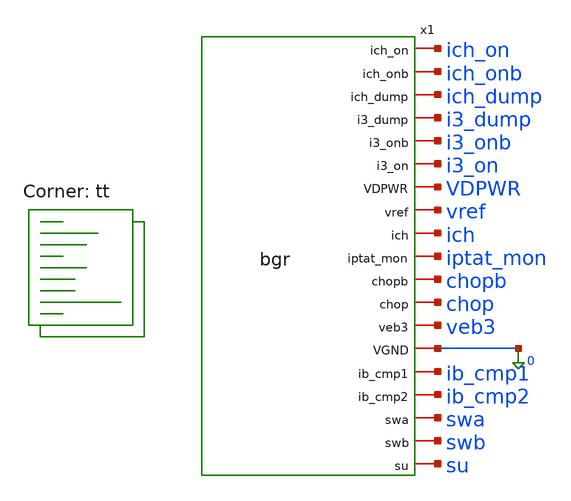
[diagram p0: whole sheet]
** sch_path: xschem/tb_bg_chop.sch
**.subckt tb_bg_chop
x1 ich_on ich_onb ich_dump i3_dump i3_onb i3_on VDPWR vref ich iptat_mon chopb chop veb3 0 ib_cmp1
+ ib_cmp2 swa swb su bgr
**** begin user architecture code
.lib $::SKYWATER_MODELS/sky130.lib.spice tt

*   S0 = normal, S1 = i3_sel 1 (half-current output branch), S2 = ich_sel 1 (half slope)
Vdd VDPWR 0 1.8
Vswa swa 0 1.8
Vswb swb 0 0
Vchop chop 0 0
Vchopb chopb 0 1.8
Vichon ich_on 0 1.8
Vichonb ich_onb 0 0
Vichdump ich_dump 0 0
Vi3on i3_on 0 1.8
Vi3onb i3_onb 0 0
Vi3dump i3_dump 0 0
* parks as in 3d; 2 pF on vref as the spec bench
E4 p4 0 x1.va 0 1
V4 ich p4 0
V7 iptat_mon p4 0
Vc1 ib_cmp1 0 0.70
Vc2 ib_cmp2 0 0.70
Cref vref 0 2p
* the design nodeset
.nodeset v(x1.vpg)=0.55 v(x1.va)=0.71 v(x1.vb)=0.71 v(vref)=1.25
.control
option reltol=1e-6 vntol=1e-9 abstol=1e-15
let vd = 1.8
foreach t -40 -20 0 25 50 75 100 125
  option temp=$t
  * S0: normal
  op
  let ip = 2*i(v7)*1e9
  let ib = abs(@m.x1.xcore.xmnb2.msky130_fd_pr__nfet_01v8[id])*1e9
  let ibr = ib/ip
  let xvref = v(vref)
  let xveb3 = v(veb3)
  let mu = 1 - xveb3/xvref
  let vos = (v(x1.vb)-v(x1.va))*1e6
  let xvpg = v(x1.vpg)
  let tailm = (abs(@m.x1.xota.xmtail.msky130_fd_pr__pfet_01v8[vds]) -
+ abs(@m.x1.xota.xmtail.msky130_fd_pr__pfet_01v8[vdsat]))*1e3
  let p3m = (abs(@m.x1.xcore.x1.xmp3a.msky130_fd_pr__pfet_01v8[vds]) -
+ abs(@m.x1.xcore.x1.xmp3a.msky130_fd_pr__pfet_01v8[vdsat]))*1e3
  let xsu = v(su)*1e3
  let imsu1 = abs(@m.x1.xcore.xsu.xmsu1.msky130_fd_pr__pfet_01v8[id])*1e9
  let imsu2 = abs(@m.x1.xcore.xsu.xmsu2.msky130_fd_pr__nfet_01v8[id])*1e12
  let ich = i(v4)*1e9
  set s0vref = $&xvref
  set s0veb3 = $&xveb3
  set s0ich = $&ich
  let i3s0 = abs(@m.x1.xcore.x1.xmp3a.msky130_fd_pr__pfet_01v8[id]) +
+ abs(@m.x1.xcore.x1.xmp3b.msky130_fd_pr__pfet_01v8[id])
  set s0i3 = $&i3s0
  echo PVT temp=$t Iptat_nA=$&ip IB_ratio=$&ibr vref_V=$&xvref veb3_V=$&xveb3 mu=$&mu vos_uV=$&vos
+ vpg_V=$&xvpg tail_margin_mV=$&tailm p3_margin_mV=$&p3m su_mV=$&xsu Imsu1_nA=$&imsu1 Imsu2_pA=$&imsu2
+ Ich_nA=$&ich
  * 8c: input-switch leakage, state A (S1/S2 on, S3/S4 off): everything hanging on va and vb
  let lva = (abs(@m.x1.xs1.msky130_fd_pr__nfet_01v8_lvt[id]) +
+ abs(@m.x1.xs1.msky130_fd_pr__nfet_01v8_lvt[ibd]) + abs(@m.x1.xs3.msky130_fd_pr__nfet_01v8_lvt[id]) +
+ abs(@m.x1.xs3.msky130_fd_pr__nfet_01v8_lvt[ibd]))*1e12
  let lvb = (abs(@m.x1.xs2.msky130_fd_pr__nfet_01v8_lvt[id]) +
+ abs(@m.x1.xs2.msky130_fd_pr__nfet_01v8_lvt[ibd]) + abs(@m.x1.xs4.msky130_fd_pr__nfet_01v8_lvt[id]) +
+ abs(@m.x1.xs4.msky130_fd_pr__nfet_01v8_lvt[ibd]))*1e12
  let loff = abs(@m.x1.xs3.msky130_fd_pr__nfet_01v8_lvt[id])*1e12
  echo LEAK temp=$t Ileak_va_pA=$&lva Ileak_vb_pA=$&lvb Ioff_channel_S3_pA=$&loff
  * S1: i3_sel = 1 (P3b to ground)
  alter vi3on = 0
  alter vi3onb = $&vd
  alter vi3dump = $&vd
  op
  let i3a = abs(@m.x1.xcore.x1.xmp3a.msky130_fd_pr__pfet_01v8[id])
  let rho = i3a/$s0i3
  let xvref = v(vref)
  let xveb3 = v(veb3)
  let mu = 1 - xveb3/xvref
  let xsu = v(su)*1e3
  let chi = 10*$s0veb3/($s0vref - $s0veb3) - 5*xveb3/(xvref - xveb3) - 1/3
  echo HALF temp=$t rho=$&rho vref_V=$&xvref veb3_V=$&xveb3 mu=$&mu su_mV=$&xsu chi_nom=$&chi
  alter vi3on = $&vd
  alter vi3onb = 0
  alter vi3dump = 0
  * S2: ich_sel = 1 (P4b to ground)
  alter vichon = 0
  alter vichonb = $&vd
  alter vichdump = $&vd
  op
  let ich = i(v4)*1e9
  let ichr = ich/$s0ich
  echo SLOPE temp=$t Ich_nA=$&ich Ich_ratio=$&ichr
  alter vichon = $&vd
  alter vichonb = 0
  alter vichdump = 0
end
.endc

**** end user architecture code
**.ends

* expanding   symbol:  bgr.sym # of pins=19
** sym_path: xschem/bgr.sym
** sch_path: xschem/bgr.sch
.subckt bgr ich_on ich_onb ich_dump i3_dump i3_onb i3_on VDPWR vref ich iptat_mon chopb chop veb3
+ VGND ib_cmp1 ib_cmp2 swa swb su
*.iopin swb
*.iopin VDPWR
*.iopin VGND
*.iopin vref
*.iopin veb3
*.iopin ich
*.iopin iptat_mon
*.iopin ib_cmp1
*.iopin ib_cmp2
*.iopin swa
*.iopin chop
*.iopin chopb
*.iopin ich_on
*.iopin ich_onb
*.iopin ich_dump
*.iopin i3_on
*.iopin i3_onb
*.iopin i3_dump
*.iopin su
xcore vpg VDPWR i3b vref ichb ich vb iptat_mon veb3 VGND va ibias ib_cmp1 ib_cmp2 su bg_core
xota inp inn vpg VDPWR VGND ibias chop chopb ota2s
XS1 va swa inn VGND sky130_fd_pr__nfet_01v8_lvt L=0.5 W=4 nf=1 ad='int((1 + 1)/2) * 4 / 1 * 0.29' as='int((1 + 2)/2) * 4 / 1 * 0.29'
+ pd='2*int((1 + 1)/2) * (4 / 1 + 0.29)' ps='2*int((1 + 2)/2) * (4 / 1 + 0.29)' nrd='0.29 / 4 ' nrs='0.29 / 4 '
+ sa=0 sb=0 sd=0 mult=1 m=1
XS2 vb swa inp VGND sky130_fd_pr__nfet_01v8_lvt L=0.5 W=4 nf=1 ad='int((1 + 1)/2) * 4 / 1 * 0.29' as='int((1 + 2)/2) * 4 / 1 * 0.29'
+ pd='2*int((1 + 1)/2) * (4 / 1 + 0.29)' ps='2*int((1 + 2)/2) * (4 / 1 + 0.29)' nrd='0.29 / 4 ' nrs='0.29 / 4 '
+ sa=0 sb=0 sd=0 mult=1 m=1
XS3 va swb inp VGND sky130_fd_pr__nfet_01v8_lvt L=0.5 W=4 nf=1 ad='int((1 + 1)/2) * 4 / 1 * 0.29' as='int((1 + 2)/2) * 4 / 1 * 0.29'
+ pd='2*int((1 + 1)/2) * (4 / 1 + 0.29)' ps='2*int((1 + 2)/2) * (4 / 1 + 0.29)' nrd='0.29 / 4 ' nrs='0.29 / 4 '
+ sa=0 sb=0 sd=0 mult=1 m=1
XS4 vb swb inn VGND sky130_fd_pr__nfet_01v8_lvt L=0.5 W=4 nf=1 ad='int((1 + 1)/2) * 4 / 1 * 0.29' as='int((1 + 2)/2) * 4 / 1 * 0.29'
+ pd='2*int((1 + 1)/2) * (4 / 1 + 0.29)' ps='2*int((1 + 2)/2) * (4 / 1 + 0.29)' nrd='0.29 / 4 ' nrs='0.29 / 4 '
+ sa=0 sb=0 sd=0 mult=1 m=1
XS_ichon_n ichb ich_on ich VGND sky130_fd_pr__nfet_01v8 L=0.5 W=2 nf=1 ad='int((1 + 1)/2) * 2 / 1 * 0.29'
+ as='int((1 + 2)/2) * 2 / 1 * 0.29' pd='2*int((1 + 1)/2) * (2 / 1 + 0.29)' ps='2*int((1 + 2)/2) * (2 / 1 + 0.29)'
+ nrd='0.29 / 2 ' nrs='0.29 / 2 ' sa=0 sb=0 sd=0 mult=1 m=1
XS_ichon_p ichb ich_onb ich VDPWR sky130_fd_pr__pfet_01v8 L=0.5 W=4 nf=1 ad='int((1 + 1)/2) * 4 / 1 * 0.29'
+ as='int((1 + 2)/2) * 4 / 1 * 0.29' pd='2*int((1 + 1)/2) * (4 / 1 + 0.29)' ps='2*int((1 + 2)/2) * (4 / 1 + 0.29)'
+ nrd='0.29 / 4 ' nrs='0.29 / 4 ' sa=0 sb=0 sd=0 mult=1 m=1
XS_ichdump ichb ich_dump VGND VGND sky130_fd_pr__nfet_01v8 L=0.5 W=1 nf=1 ad='int((1 + 1)/2) * 1 / 1 * 0.29'
+ as='int((1 + 2)/2) * 1 / 1 * 0.29' pd='2*int((1 + 1)/2) * (1 / 1 + 0.29)' ps='2*int((1 + 2)/2) * (1 / 1 + 0.29)'
+ nrd='0.29 / 1 ' nrs='0.29 / 1 ' sa=0 sb=0 sd=0 mult=1 m=1
XS_i3on_n i3b i3_on vref VGND sky130_fd_pr__nfet_01v8 L=0.5 W=2 nf=1 ad='int((1 + 1)/2) * 2 / 1 * 0.29'
+ as='int((1 + 2)/2) * 2 / 1 * 0.29' pd='2*int((1 + 1)/2) * (2 / 1 + 0.29)' ps='2*int((1 + 2)/2) * (2 / 1 + 0.29)'
+ nrd='0.29 / 2 ' nrs='0.29 / 2 ' sa=0 sb=0 sd=0 mult=1 m=1
XS_i3on_p i3b i3_onb vref VDPWR sky130_fd_pr__pfet_01v8 L=0.5 W=4 nf=1 ad='int((1 + 1)/2) * 4 / 1 * 0.29'
+ as='int((1 + 2)/2) * 4 / 1 * 0.29' pd='2*int((1 + 1)/2) * (4 / 1 + 0.29)' ps='2*int((1 + 2)/2) * (4 / 1 + 0.29)'
+ nrd='0.29 / 4 ' nrs='0.29 / 4 ' sa=0 sb=0 sd=0 mult=1 m=1
XS_i3dump i3b i3_dump VGND VGND sky130_fd_pr__nfet_01v8 L=0.5 W=1 nf=1 ad='int((1 + 1)/2) * 1 / 1 * 0.29'
+ as='int((1 + 2)/2) * 1 / 1 * 0.29' pd='2*int((1 + 1)/2) * (1 / 1 + 0.29)' ps='2*int((1 + 2)/2) * (1 / 1 + 0.29)'
+ nrd='0.29 / 1 ' nrs='0.29 / 1 ' sa=0 sb=0 sd=0 mult=1 m=1
.ends


* expanding   symbol:  bg_core.sym # of pins=15
** sym_path: xschem/bg_core.sym
** sch_path: xschem/bg_core.sch
.subckt bg_core vpg VDPWR i3b vref ichb ich vb iptat_mon veb3 VGND va ibias ib_cmp1 ib_cmp2 su
*.iopin va
*.iopin vb
*.iopin vref
*.iopin veb3
*.iopin vpg
*.iopin i3b
*.iopin VDPWR
*.iopin ichb
*.iopin ich
*.iopin iptat_mon
*.iopin ibias
*.iopin ib_cmp1
*.iopin ib_cmp2
*.iopin VGND
*.iopin su
x1 vpg VDPWR i3b vref ichb ich vb iptat_mon nb va bg_mirror
x2 vb vref veb3 VGND eb2 bg_rrow
x3 va veb3 eb2 VGND bg_pnp
XMNB1 nb nb VGND VGND sky130_fd_pr__nfet_01v8 L=8 W=4 nf=1 ad='int((1 + 1)/2) * 4 / 1 * 0.29' as='int((1 + 2)/2) * 4 / 1 * 0.29'
+ pd='2*int((1 + 1)/2) * (4 / 1 + 0.29)' ps='2*int((1 + 2)/2) * (4 / 1 + 0.29)' nrd='0.29 / 4 ' nrs='0.29 / 4 '
+ sa=0 sb=0 sd=0 mult=1 m=1
XMNB2 ibias nb VGND VGND sky130_fd_pr__nfet_01v8 L=8 W=4 nf=1 ad='int((1 + 1)/2) * 4 / 1 * 0.29' as='int((1 + 2)/2) * 4 / 1 * 0.29'
+ pd='2*int((1 + 1)/2) * (4 / 1 + 0.29)' ps='2*int((1 + 2)/2) * (4 / 1 + 0.29)' nrd='0.29 / 4 ' nrs='0.29 / 4 '
+ sa=0 sb=0 sd=0 mult=1 m=1
XMNB3 ib_cmp1 nb VGND VGND sky130_fd_pr__nfet_01v8 L=8 W=4 nf=1 ad='int((1 + 1)/2) * 4 / 1 * 0.29' as='int((1 + 2)/2) * 4 / 1 * 0.29'
+ pd='2*int((1 + 1)/2) * (4 / 1 + 0.29)' ps='2*int((1 + 2)/2) * (4 / 1 + 0.29)' nrd='0.29 / 4 ' nrs='0.29 / 4 '
+ sa=0 sb=0 sd=0 mult=4 m=4
XMNB4 ib_cmp2 nb VGND VGND sky130_fd_pr__nfet_01v8 L=8 W=4 nf=1 ad='int((1 + 1)/2) * 4 / 1 * 0.29' as='int((1 + 2)/2) * 4 / 1 * 0.29'
+ pd='2*int((1 + 1)/2) * (4 / 1 + 0.29)' ps='2*int((1 + 2)/2) * (4 / 1 + 0.29)' nrd='0.29 / 4 ' nrs='0.29 / 4 '
+ sa=0 sb=0 sd=0 mult=4 m=4
xsu VDPWR vref vpg su VGND nb bg_su
.ends


* expanding   symbol:  ota2s.sym # of pins=8
** sym_path: xschem/ota2s.sym
** sch_path: xschem/ota2s.sch
.subckt ota2s INP INN OUT VDPWR VGND IBIAS CHOP CHOPB
*.ipin INN
*.ipin INP
*.ipin IBIAS
*.opin OUT
*.iopin VDPWR
*.iopin VGND
*.ipin CHOPB
*.ipin CHOP
XMREF IBIAS IBIAS VDPWR VDPWR sky130_fd_pr__pfet_01v8 L=4 W=20 nf=1 ad='int((1 + 1)/2) * 20 / 1 * 0.29'
+ as='int((1 + 2)/2) * 20 / 1 * 0.29' pd='2*int((1 + 1)/2) * (20 / 1 + 0.29)' ps='2*int((1 + 2)/2) * (20 / 1 + 0.29)'
+ nrd='0.29 / 20 ' nrs='0.29 / 20 ' sa=0 sb=0 sd=0 mult=1 m=1
XMTAIL tail IBIAS VDPWR VDPWR sky130_fd_pr__pfet_01v8 L=4 W=20 nf=1 ad='int((1 + 1)/2) * 20 / 1 * 0.29'
+ as='int((1 + 2)/2) * 20 / 1 * 0.29' pd='2*int((1 + 1)/2) * (20 / 1 + 0.29)' ps='2*int((1 + 2)/2) * (20 / 1 + 0.29)'
+ nrd='0.29 / 20 ' nrs='0.29 / 20 ' sa=0 sb=0 sd=0 mult=2 m=2
XMP1 d1 INN tail VDPWR sky130_fd_pr__pfet_01v8_lvt L=6 W=25 nf=1 ad='int((1 + 1)/2) * 25 / 1 * 0.29'
+ as='int((1 + 2)/2) * 25 / 1 * 0.29' pd='2*int((1 + 1)/2) * (25 / 1 + 0.29)' ps='2*int((1 + 2)/2) * (25 / 1 + 0.29)'
+ nrd='0.29 / 25 ' nrs='0.29 / 25 ' sa=0 sb=0 sd=0 mult=24 m=24
XMP2 x1 INP tail VDPWR sky130_fd_pr__pfet_01v8_lvt L=6 W=25 nf=1 ad='int((1 + 1)/2) * 25 / 1 * 0.29'
+ as='int((1 + 2)/2) * 25 / 1 * 0.29' pd='2*int((1 + 1)/2) * (25 / 1 + 0.29)' ps='2*int((1 + 2)/2) * (25 / 1 + 0.29)'
+ nrd='0.29 / 25 ' nrs='0.29 / 25 ' sa=0 sb=0 sd=0 mult=24 m=24
XMN1 d1 g12 VGND VGND sky130_fd_pr__nfet_01v8 L=20 W=6 nf=1 ad='int((1 + 1)/2) * 6 / 1 * 0.29' as='int((1 + 2)/2) * 6 / 1 * 0.29'
+ pd='2*int((1 + 1)/2) * (6 / 1 + 0.29)' ps='2*int((1 + 2)/2) * (6 / 1 + 0.29)' nrd='0.29 / 6 ' nrs='0.29 / 6 '
+ sa=0 sb=0 sd=0 mult=2 m=2
XMN2 x1 g12 VGND VGND sky130_fd_pr__nfet_01v8 L=20 W=6 nf=1 ad='int((1 + 1)/2) * 6 / 1 * 0.29' as='int((1 + 2)/2) * 6 / 1 * 0.29'
+ pd='2*int((1 + 1)/2) * (6 / 1 + 0.29)' ps='2*int((1 + 2)/2) * (6 / 1 + 0.29)' nrd='0.29 / 6 ' nrs='0.29 / 6 '
+ sa=0 sb=0 sd=0 mult=2 m=2
XMP3 OUT IBIAS VDPWR VDPWR sky130_fd_pr__pfet_01v8 L=4 W=20 nf=1 ad='int((1 + 1)/2) * 20 / 1 * 0.29'
+ as='int((1 + 2)/2) * 20 / 1 * 0.29' pd='2*int((1 + 1)/2) * (20 / 1 + 0.29)' ps='2*int((1 + 2)/2) * (20 / 1 + 0.29)'
+ nrd='0.29 / 20 ' nrs='0.29 / 20 ' sa=0 sb=0 sd=0 mult=6 m=6
XMN3 OUT g3 VGND VGND sky130_fd_pr__nfet_01v8 L=1 W=7 nf=1 ad='int((1 + 1)/2) * 7 / 1 * 0.29' as='int((1 + 2)/2) * 7 / 1 * 0.29'
+ pd='2*int((1 + 1)/2) * (7 / 1 + 0.29)' ps='2*int((1 + 2)/2) * (7 / 1 + 0.29)' nrd='0.29 / 7 ' nrs='0.29 / 7 '
+ sa=0 sb=0 sd=0 mult=1 m=1
XRZ1 net1 g3 VGND sky130_fd_pr__res_high_po_1p41 L=20 mult=1 m=1
XRZ2 net2 net1 VGND sky130_fd_pr__res_high_po_1p41 L=20 mult=1 m=1
XRZ3 net3 net2 VGND sky130_fd_pr__res_high_po_1p41 L=20 mult=1 m=1
XRZ4 net4 net3 VGND sky130_fd_pr__res_high_po_1p41 L=20 mult=1 m=1
XRZ5 net5 net4 VGND sky130_fd_pr__res_high_po_1p41 L=20 mult=1 m=1
XRZ6 cz net5 VGND sky130_fd_pr__res_high_po_1p41 L=20 mult=1 m=1
XCC cz OUT sky130_fd_pr__cap_mim_m3_1 W=25 L=25 MF=8 m=8
XDP tail VDPWR tail VDPWR sky130_fd_pr__pfet_01v8_lvt L=6 W=25 nf=1 ad='int((1 + 1)/2) * 25 / 1 * 0.29'
+ as='int((1 + 2)/2) * 25 / 1 * 0.29' pd='2*int((1 + 1)/2) * (25 / 1 + 0.29)' ps='2*int((1 + 2)/2) * (25 / 1 + 0.29)'
+ nrd='0.29 / 25 ' nrs='0.29 / 25 ' sa=0 sb=0 sd=0 mult=8 m=8
XDNA d1 VGND VGND VGND sky130_fd_pr__nfet_01v8 L=20 W=6 nf=1 ad='int((1 + 1)/2) * 6 / 1 * 0.29' as='int((1 + 2)/2) * 6 / 1 * 0.29'
+ pd='2*int((1 + 1)/2) * (6 / 1 + 0.29)' ps='2*int((1 + 2)/2) * (6 / 1 + 0.29)' nrd='0.29 / 6 ' nrs='0.29 / 6 '
+ sa=0 sb=0 sd=0 mult=2 m=2
XDNB x1 VGND VGND VGND sky130_fd_pr__nfet_01v8 L=20 W=6 nf=1 ad='int((1 + 1)/2) * 6 / 1 * 0.29' as='int((1 + 2)/2) * 6 / 1 * 0.29'
+ pd='2*int((1 + 1)/2) * (6 / 1 + 0.29)' ps='2*int((1 + 2)/2) * (6 / 1 + 0.29)' nrd='0.29 / 6 ' nrs='0.29 / 6 '
+ sa=0 sb=0 sd=0 mult=2 m=2
XDB VDPWR VDPWR VDPWR VDPWR sky130_fd_pr__pfet_01v8 L=4 W=20 nf=1 ad='int((1 + 1)/2) * 20 / 1 * 0.29'
+ as='int((1 + 2)/2) * 20 / 1 * 0.29' pd='2*int((1 + 1)/2) * (20 / 1 + 0.29)' ps='2*int((1 + 2)/2) * (20 / 1 + 0.29)'
+ nrd='0.29 / 20 ' nrs='0.29 / 20 ' sa=0 sb=0 sd=0 mult=2 m=2
XRD1 VGND VGND VGND sky130_fd_pr__res_high_po_1p41 L=20 mult=1 m=1
XRD2 VGND VGND VGND sky130_fd_pr__res_high_po_1p41 L=20 mult=1 m=1
XSD1 d1 CHOPB g12 VGND sky130_fd_pr__nfet_01v8 L=0.5 W=6 nf=1 ad='int((1 + 1)/2) * 6 / 1 * 0.29' as='int((1 + 2)/2) * 6 / 1 * 0.29'
+ pd='2*int((1 + 1)/2) * (6 / 1 + 0.29)' ps='2*int((1 + 2)/2) * (6 / 1 + 0.29)' nrd='0.29 / 6 ' nrs='0.29 / 6 '
+ sa=0 sb=0 sd=0 mult=1 m=1
XSD2 x1 CHOP g12 VGND sky130_fd_pr__nfet_01v8 L=0.5 W=6 nf=1 ad='int((1 + 1)/2) * 6 / 1 * 0.29' as='int((1 + 2)/2) * 6 / 1 * 0.29'
+ pd='2*int((1 + 1)/2) * (6 / 1 + 0.29)' ps='2*int((1 + 2)/2) * (6 / 1 + 0.29)' nrd='0.29 / 6 ' nrs='0.29 / 6 '
+ sa=0 sb=0 sd=0 mult=1 m=1
XSG2 g3 CHOP d1 VGND sky130_fd_pr__nfet_01v8 L=0.5 W=6 nf=1 ad='int((1 + 1)/2) * 6 / 1 * 0.29' as='int((1 + 2)/2) * 6 / 1 * 0.29'
+ pd='2*int((1 + 1)/2) * (6 / 1 + 0.29)' ps='2*int((1 + 2)/2) * (6 / 1 + 0.29)' nrd='0.29 / 6 ' nrs='0.29 / 6 '
+ sa=0 sb=0 sd=0 mult=1 m=1
XSG1 x1 CHOPB g3 VGND sky130_fd_pr__nfet_01v8 L=0.5 W=6 nf=1 ad='int((1 + 1)/2) * 6 / 1 * 0.29' as='int((1 + 2)/2) * 6 / 1 * 0.29'
+ pd='2*int((1 + 1)/2) * (6 / 1 + 0.29)' ps='2*int((1 + 2)/2) * (6 / 1 + 0.29)' nrd='0.29 / 6 ' nrs='0.29 / 6 '
+ sa=0 sb=0 sd=0 mult=1 m=1
.ends


* expanding   symbol:  bg_mirror.sym # of pins=10
** sym_path: xschem/bg_mirror.sym
** sch_path: xschem/bg_mirror.sch
.subckt bg_mirror vpg VDPWR d3b d3a d4b d4a d2 d7 d5 d1
*.iopin vpg
*.iopin VDPWR
*.iopin d1
*.iopin d2
*.iopin d3a
*.iopin d3b
*.iopin d4a
*.iopin d4b
*.iopin d7
*.iopin d5
XMP1 d1 vpg VDPWR VDPWR sky130_fd_pr__pfet_01v8 L=20 W=8.8 nf=1 ad='int((1 + 1)/2) * 8.8 / 1 * 0.29'
+ as='int((1 + 2)/2) * 8.8 / 1 * 0.29' pd='2*int((1 + 1)/2) * (8.8 / 1 + 0.29)' ps='2*int((1 + 2)/2) * (8.8 / 1 + 0.29)'
+ nrd='0.29 / 8.8 ' nrs='0.29 / 8.8 ' sa=0 sb=0 sd=0 mult=4 m=4
XMP2 d2 vpg VDPWR VDPWR sky130_fd_pr__pfet_01v8 L=20 W=8.8 nf=1 ad='int((1 + 1)/2) * 8.8 / 1 * 0.29'
+ as='int((1 + 2)/2) * 8.8 / 1 * 0.29' pd='2*int((1 + 1)/2) * (8.8 / 1 + 0.29)' ps='2*int((1 + 2)/2) * (8.8 / 1 + 0.29)'
+ nrd='0.29 / 8.8 ' nrs='0.29 / 8.8 ' sa=0 sb=0 sd=0 mult=4 m=4
XMP3A d3a vpg VDPWR VDPWR sky130_fd_pr__pfet_01v8 L=20 W=8.8 nf=1 ad='int((1 + 1)/2) * 8.8 / 1 * 0.29'
+ as='int((1 + 2)/2) * 8.8 / 1 * 0.29' pd='2*int((1 + 1)/2) * (8.8 / 1 + 0.29)' ps='2*int((1 + 2)/2) * (8.8 / 1 + 0.29)'
+ nrd='0.29 / 8.8 ' nrs='0.29 / 8.8 ' sa=0 sb=0 sd=0 mult=2 m=2
XMP3B d3b vpg VDPWR VDPWR sky130_fd_pr__pfet_01v8 L=20 W=8.8 nf=1 ad='int((1 + 1)/2) * 8.8 / 1 * 0.29'
+ as='int((1 + 2)/2) * 8.8 / 1 * 0.29' pd='2*int((1 + 1)/2) * (8.8 / 1 + 0.29)' ps='2*int((1 + 2)/2) * (8.8 / 1 + 0.29)'
+ nrd='0.29 / 8.8 ' nrs='0.29 / 8.8 ' sa=0 sb=0 sd=0 mult=2 m=2
XMP4A d4a vpg VDPWR VDPWR sky130_fd_pr__pfet_01v8 L=20 W=8.8 nf=1 ad='int((1 + 1)/2) * 8.8 / 1 * 0.29'
+ as='int((1 + 2)/2) * 8.8 / 1 * 0.29' pd='2*int((1 + 1)/2) * (8.8 / 1 + 0.29)' ps='2*int((1 + 2)/2) * (8.8 / 1 + 0.29)'
+ nrd='0.29 / 8.8 ' nrs='0.29 / 8.8 ' sa=0 sb=0 sd=0 mult=1 m=1
XMP4B d4b vpg VDPWR VDPWR sky130_fd_pr__pfet_01v8 L=20 W=8.8 nf=1 ad='int((1 + 1)/2) * 8.8 / 1 * 0.29'
+ as='int((1 + 2)/2) * 8.8 / 1 * 0.29' pd='2*int((1 + 1)/2) * (8.8 / 1 + 0.29)' ps='2*int((1 + 2)/2) * (8.8 / 1 + 0.29)'
+ nrd='0.29 / 8.8 ' nrs='0.29 / 8.8 ' sa=0 sb=0 sd=0 mult=1 m=1
XMP7 d7 vpg VDPWR VDPWR sky130_fd_pr__pfet_01v8 L=20 W=8.8 nf=1 ad='int((1 + 1)/2) * 8.8 / 1 * 0.29'
+ as='int((1 + 2)/2) * 8.8 / 1 * 0.29' pd='2*int((1 + 1)/2) * (8.8 / 1 + 0.29)' ps='2*int((1 + 2)/2) * (8.8 / 1 + 0.29)'
+ nrd='0.29 / 8.8 ' nrs='0.29 / 8.8 ' sa=0 sb=0 sd=0 mult=2 m=2
XMP5 d5 vpg VDPWR VDPWR sky130_fd_pr__pfet_01v8 L=20 W=8.8 nf=1 ad='int((1 + 1)/2) * 8.8 / 1 * 0.29'
+ as='int((1 + 2)/2) * 8.8 / 1 * 0.29' pd='2*int((1 + 1)/2) * (8.8 / 1 + 0.29)' ps='2*int((1 + 2)/2) * (8.8 / 1 + 0.29)'
+ nrd='0.29 / 8.8 ' nrs='0.29 / 8.8 ' sa=0 sb=0 sd=0 mult=2 m=2
.ends


* expanding   symbol:  bg_rrow.sym # of pins=5
** sym_path: xschem/bg_rrow.sym
** sch_path: xschem/bg_rrow.sch
.subckt bg_rrow vb vref veb3 VGND eb2
*.iopin vb
*.iopin eb2
*.iopin vref
*.iopin veb3
*.iopin VGND
XR1_1 eb2 net1 VGND sky130_fd_pr__res_high_po_1p41 L=20 mult=1 m=1
XR1_2 net1 net2 VGND sky130_fd_pr__res_high_po_1p41 L=20 mult=1 m=1
XR1_3 net2 net3 VGND sky130_fd_pr__res_high_po_1p41 L=20 mult=1 m=1
XR1_4 net3 vb VGND sky130_fd_pr__res_high_po_1p41 L=20 mult=1 m=1
XR3[39] r3n[38] vref VGND sky130_fd_pr__res_high_po_1p41 L=20 mult=1 m=1
XR3[38] r3n[37] r3n[38] VGND sky130_fd_pr__res_high_po_1p41 L=20 mult=1 m=1
XR3[37] r3n[36] r3n[37] VGND sky130_fd_pr__res_high_po_1p41 L=20 mult=1 m=1
XR3[36] r3n[35] r3n[36] VGND sky130_fd_pr__res_high_po_1p41 L=20 mult=1 m=1
XR3[35] r3n[34] r3n[35] VGND sky130_fd_pr__res_high_po_1p41 L=20 mult=1 m=1
XR3[34] r3n[33] r3n[34] VGND sky130_fd_pr__res_high_po_1p41 L=20 mult=1 m=1
XR3[33] r3n[32] r3n[33] VGND sky130_fd_pr__res_high_po_1p41 L=20 mult=1 m=1
XR3[32] r3n[31] r3n[32] VGND sky130_fd_pr__res_high_po_1p41 L=20 mult=1 m=1
XR3[31] r3n[30] r3n[31] VGND sky130_fd_pr__res_high_po_1p41 L=20 mult=1 m=1
XR3[30] r3n[29] r3n[30] VGND sky130_fd_pr__res_high_po_1p41 L=20 mult=1 m=1
XR3[29] r3n[28] r3n[29] VGND sky130_fd_pr__res_high_po_1p41 L=20 mult=1 m=1
XR3[28] r3n[27] r3n[28] VGND sky130_fd_pr__res_high_po_1p41 L=20 mult=1 m=1
XR3[27] r3n[26] r3n[27] VGND sky130_fd_pr__res_high_po_1p41 L=20 mult=1 m=1
XR3[26] r3n[25] r3n[26] VGND sky130_fd_pr__res_high_po_1p41 L=20 mult=1 m=1
XR3[25] r3n[24] r3n[25] VGND sky130_fd_pr__res_high_po_1p41 L=20 mult=1 m=1
XR3[24] r3n[23] r3n[24] VGND sky130_fd_pr__res_high_po_1p41 L=20 mult=1 m=1
XR3[23] r3n[22] r3n[23] VGND sky130_fd_pr__res_high_po_1p41 L=20 mult=1 m=1
XR3[22] r3n[21] r3n[22] VGND sky130_fd_pr__res_high_po_1p41 L=20 mult=1 m=1
XR3[21] r3n[20] r3n[21] VGND sky130_fd_pr__res_high_po_1p41 L=20 mult=1 m=1
XR3[20] r3n[19] r3n[20] VGND sky130_fd_pr__res_high_po_1p41 L=20 mult=1 m=1
XR3[19] r3n[18] r3n[19] VGND sky130_fd_pr__res_high_po_1p41 L=20 mult=1 m=1
XR3[18] r3n[17] r3n[18] VGND sky130_fd_pr__res_high_po_1p41 L=20 mult=1 m=1
XR3[17] r3n[16] r3n[17] VGND sky130_fd_pr__res_high_po_1p41 L=20 mult=1 m=1
XR3[16] r3n[15] r3n[16] VGND sky130_fd_pr__res_high_po_1p41 L=20 mult=1 m=1
XR3[15] r3n[14] r3n[15] VGND sky130_fd_pr__res_high_po_1p41 L=20 mult=1 m=1
XR3[14] r3n[13] r3n[14] VGND sky130_fd_pr__res_high_po_1p41 L=20 mult=1 m=1
XR3[13] r3n[12] r3n[13] VGND sky130_fd_pr__res_high_po_1p41 L=20 mult=1 m=1
XR3[12] r3n[11] r3n[12] VGND sky130_fd_pr__res_high_po_1p41 L=20 mult=1 m=1
XR3[11] r3n[10] r3n[11] VGND sky130_fd_pr__res_high_po_1p41 L=20 mult=1 m=1
XR3[10] r3n[9] r3n[10] VGND sky130_fd_pr__res_high_po_1p41 L=20 mult=1 m=1
XR3[9] r3n[8] r3n[9] VGND sky130_fd_pr__res_high_po_1p41 L=20 mult=1 m=1
XR3[8] r3n[7] r3n[8] VGND sky130_fd_pr__res_high_po_1p41 L=20 mult=1 m=1
XR3[7] r3n[6] r3n[7] VGND sky130_fd_pr__res_high_po_1p41 L=20 mult=1 m=1
XR3[6] r3n[5] r3n[6] VGND sky130_fd_pr__res_high_po_1p41 L=20 mult=1 m=1
XR3[5] r3n[4] r3n[5] VGND sky130_fd_pr__res_high_po_1p41 L=20 mult=1 m=1
XR3[4] r3n[3] r3n[4] VGND sky130_fd_pr__res_high_po_1p41 L=20 mult=1 m=1
XR3[3] r3n[2] r3n[3] VGND sky130_fd_pr__res_high_po_1p41 L=20 mult=1 m=1
XR3[2] r3n[1] r3n[2] VGND sky130_fd_pr__res_high_po_1p41 L=20 mult=1 m=1
XR3[1] r3n[0] r3n[1] VGND sky130_fd_pr__res_high_po_1p41 L=20 mult=1 m=1
XR3[0] veb3 r3n[0] VGND sky130_fd_pr__res_high_po_1p41 L=20 mult=1 m=1
XRD[3] VGND VGND VGND sky130_fd_pr__res_high_po_1p41 L=20 mult=1 m=1
XRD[2] VGND VGND VGND sky130_fd_pr__res_high_po_1p41 L=20 mult=1 m=1
XRD[1] VGND VGND VGND sky130_fd_pr__res_high_po_1p41 L=20 mult=1 m=1
XRD[0] VGND VGND VGND sky130_fd_pr__res_high_po_1p41 L=20 mult=1 m=1
.ends


* expanding   symbol:  bg_pnp.sym # of pins=4
** sym_path: xschem/bg_pnp.sym
** sch_path: xschem/bg_pnp.sch
.subckt bg_pnp va veb3 eb2 VGND
*.iopin va
*.iopin eb2
*.iopin veb3
*.iopin VGND
XQ1 VGND VGND va sky130_fd_pr__pnp_05v5_W3p40L3p40 m=1
XQ2 VGND VGND eb2 sky130_fd_pr__pnp_05v5_W3p40L3p40 m=8
XQ3 VGND VGND veb3 sky130_fd_pr__pnp_05v5_W3p40L3p40 m=1
XQD VGND VGND VGND sky130_fd_pr__pnp_05v5_W3p40L3p40 m=15
.ends


* expanding   symbol:  bg_su.sym # of pins=6
** sym_path: xschem/bg_su.sym
** sch_path: xschem/bg_su.sch
.subckt bg_su VDPWR vref vpg su VGND nb
*.iopin vref
*.iopin VGND
*.iopin vpg
*.iopin VDPWR
*.iopin su
*.iopin nb
XMSU1 su vref VDPWR VDPWR sky130_fd_pr__pfet_01v8 L=20 W=0.42 nf=1 ad='int((1 + 1)/2) * 0.42 / 1 * 0.29'
+ as='int((1 + 2)/2) * 0.42 / 1 * 0.29' pd='2*int((1 + 1)/2) * (0.42 / 1 + 0.29)' ps='2*int((1 + 2)/2) * (0.42 / 1 + 0.29)'
+ nrd='0.29 / 0.42 ' nrs='0.29 / 0.42 ' sa=0 sb=0 sd=0 mult=1 m=1
XMSU3 su nb VGND VGND sky130_fd_pr__nfet_01v8 L=1 W=0.42 nf=1 ad='int((1 + 1)/2) * 0.42 / 1 * 0.29' as='int((1 + 2)/2) * 0.42 / 1 * 0.29'
+ pd='2*int((1 + 1)/2) * (0.42 / 1 + 0.29)' ps='2*int((1 + 2)/2) * (0.42 / 1 + 0.29)' nrd='0.29 / 0.42 '
+ nrs='0.29 / 0.42 ' sa=0 sb=0 sd=0 mult=1 m=1
XMSU2 vpg su VGND VGND sky130_fd_pr__nfet_01v8 L=10 W=0.42 nf=1 ad='int((1 + 1)/2) * 0.42 / 1 * 0.29'
+ as='int((1 + 2)/2) * 0.42 / 1 * 0.29' pd='2*int((1 + 1)/2) * (0.42 / 1 + 0.29)' ps='2*int((1 + 2)/2) * (0.42 / 1 + 0.29)'
+ nrd='0.29 / 0.42 ' nrs='0.29 / 0.42 ' sa=0 sb=0 sd=0 mult=1 m=1
.ends

.end
